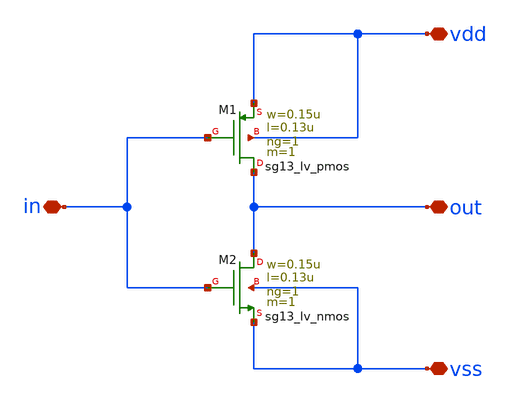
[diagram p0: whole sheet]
** sch_path: design/blocks/inverter/schematic/inverter.sch
**.subckt inverter in out vss vdd
*.iopin in
*.iopin out
*.iopin vss
*.iopin vdd
XM1 out in vdd vdd sg13_lv_pmos w=0.15u l=0.13u ng=1 m=1 mm_ok=1
XM2 out in vss vss sg13_lv_nmos w=0.15u l=0.13u ng=1 m=1 mm_ok=1
**.ends
.end
